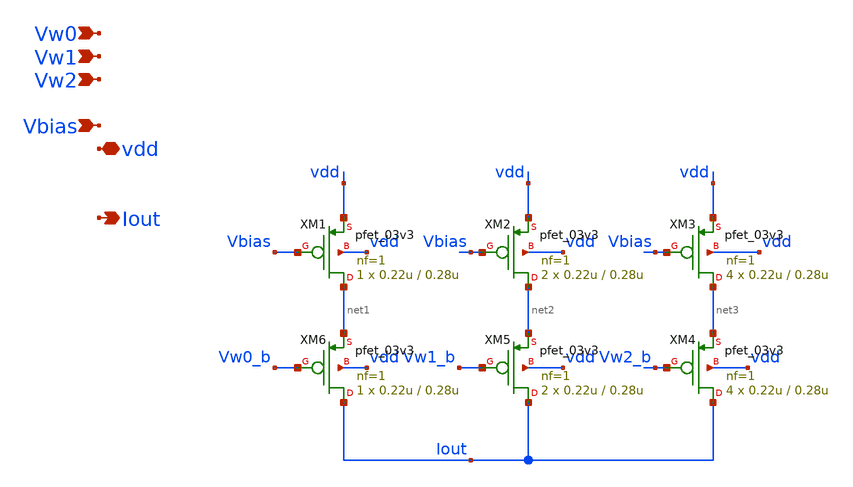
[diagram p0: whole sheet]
** sch_path: analog/dac/3bit_PMOS_DAC.sch
**.subckt 3bit_PMOS_DAC Vw0 vdd Iout Vw1 Vw2 Vbias
*.ipin Vw0
*.iopin vdd
*.opin Iout
*.ipin Vw1
*.ipin Vw2
*.ipin Vbias
XM1 net1 Vbias vdd vdd pfet_03v3 L=0.28u W=0.22u nf=1 ad='int((nf+1)/2) * W/nf * 0.18u' as='int((nf+2)/2) * W/nf * 0.18u'
+ pd='2*int((nf+1)/2) * (W/nf + 0.18u)' ps='2*int((nf+2)/2) * (W/nf + 0.18u)' nrd='0.18u / W' nrs='0.18u / W'
+ sa=0 sb=0 sd=0 m=1
XM2 net2 Vbias vdd vdd pfet_03v3 L=0.28u W=0.22u nf=1 ad='int((nf+1)/2) * W/nf * 0.18u' as='int((nf+2)/2) * W/nf * 0.18u'
+ pd='2*int((nf+1)/2) * (W/nf + 0.18u)' ps='2*int((nf+2)/2) * (W/nf + 0.18u)' nrd='0.18u / W' nrs='0.18u / W'
+ sa=0 sb=0 sd=0 m=2
XM3 net3 Vbias vdd vdd pfet_03v3 L=0.28u W=0.22u nf=1 ad='int((nf+1)/2) * W/nf * 0.18u' as='int((nf+2)/2) * W/nf * 0.18u'
+ pd='2*int((nf+1)/2) * (W/nf + 0.18u)' ps='2*int((nf+2)/2) * (W/nf + 0.18u)' nrd='0.18u / W' nrs='0.18u / W'
+ sa=0 sb=0 sd=0 m=4
XM4 Iout Vw2_b net3 vdd pfet_03v3 L=0.28u W=0.22u nf=1 ad='int((nf+1)/2) * W/nf * 0.18u' as='int((nf+2)/2) * W/nf * 0.18u'
+ pd='2*int((nf+1)/2) * (W/nf + 0.18u)' ps='2*int((nf+2)/2) * (W/nf + 0.18u)' nrd='0.18u / W' nrs='0.18u / W'
+ sa=0 sb=0 sd=0 m=4
XM5 Iout Vw1_b net2 vdd pfet_03v3 L=0.28u W=0.22u nf=1 ad='int((nf+1)/2) * W/nf * 0.18u' as='int((nf+2)/2) * W/nf * 0.18u'
+ pd='2*int((nf+1)/2) * (W/nf + 0.18u)' ps='2*int((nf+2)/2) * (W/nf + 0.18u)' nrd='0.18u / W' nrs='0.18u / W'
+ sa=0 sb=0 sd=0 m=2
XM6 Iout Vw0_b net1 vdd pfet_03v3 L=0.28u W=0.22u nf=1 ad='int((nf+1)/2) * W/nf * 0.18u' as='int((nf+2)/2) * W/nf * 0.18u'
+ pd='2*int((nf+1)/2) * (W/nf + 0.18u)' ps='2*int((nf+2)/2) * (W/nf + 0.18u)' nrd='0.18u / W' nrs='0.18u / W'
+ sa=0 sb=0 sd=0 m=1
**.ends
.end
